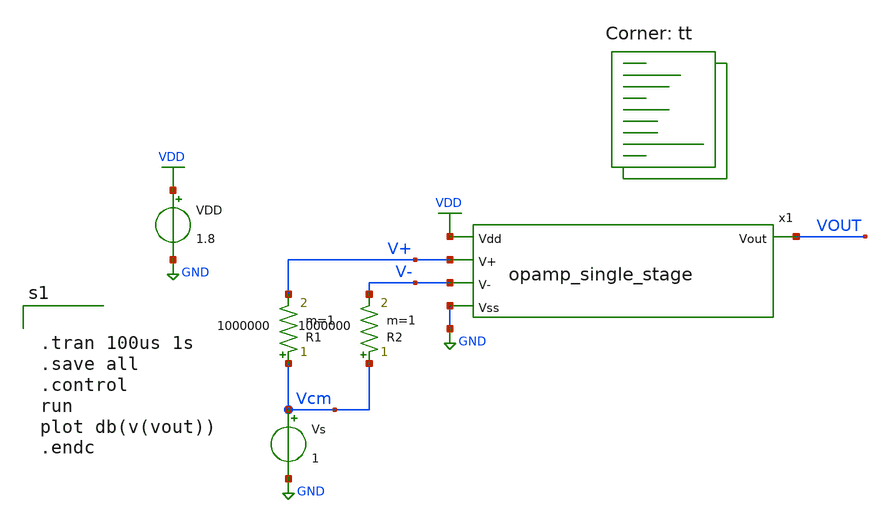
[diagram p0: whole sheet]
** sch_path: analog/schematics/tb_cmrr.sch
**.subckt tb_cmrr
VDD VDD GND 1.8
Vs Vcm GND 1
R1 Vcm V+ 1000000 m=1
R2 Vcm V- 1000000 m=1
x1 VDD VOUT V+ V- GND opamp_single_stage
**** begin user architecture code


.tran 100us 1s
.save all
.control
run
plot db(v(vout))
.endc


.lib $::SKYWATER_MODELS/sky130.lib.spice tt
**** end user architecture code
**.ends

* expanding   symbol:  opamp_single_stage.sym # of pins=5
** sym_path: analog/schematics/opamp_single_stage.sym
** sch_path: analog/schematics/opamp_single_stage.sch
.subckt opamp_single_stage Vdd Vout V+ V- Vss
*.opin Vout
*.ipin Vdd
*.ipin Vss
*.ipin V+
*.ipin V-
XM3 net1 V+ net2 Vss sky130_fd_pr__nfet_01v8 L=0.25 W=1 nf=1 ad='int((nf+1)/2) * W/nf * 0.29' as='int((nf+2)/2) * W/nf * 0.29'
+ pd='2*int((nf+1)/2) * (W/nf + 0.29)' ps='2*int((nf+2)/2) * (W/nf + 0.29)' nrd='0.29 / W' nrs='0.29 / W'
+ sa=0 sb=0 sd=0 mult=1 m=1
XM4 Vout V- net2 Vss sky130_fd_pr__nfet_01v8 L=0.25 W=1 nf=1 ad='int((nf+1)/2) * W/nf * 0.29' as='int((nf+2)/2) * W/nf * 0.29'
+ pd='2*int((nf+1)/2) * (W/nf + 0.29)' ps='2*int((nf+2)/2) * (W/nf + 0.29)' nrd='0.29 / W' nrs='0.29 / W'
+ sa=0 sb=0 sd=0 mult=1 m=1
XM5 net2 net3 Vss Vss sky130_fd_pr__nfet_01v8 L=0.25 W=1 nf=1 ad='int((nf+1)/2) * W/nf * 0.29' as='int((nf+2)/2) * W/nf * 0.29'
+ pd='2*int((nf+1)/2) * (W/nf + 0.29)' ps='2*int((nf+2)/2) * (W/nf + 0.29)' nrd='0.29 / W' nrs='0.29 / W'
+ sa=0 sb=0 sd=0 mult=1 m=1
XM1 net1 net1 Vdd Vdd sky130_fd_pr__pfet_01v8 L=0.25 W=1 nf=1 ad='int((nf+1)/2) * W/nf * 0.29' as='int((nf+2)/2) * W/nf * 0.29'
+ pd='2*int((nf+1)/2) * (W/nf + 0.29)' ps='2*int((nf+2)/2) * (W/nf + 0.29)' nrd='0.29 / W' nrs='0.29 / W'
+ sa=0 sb=0 sd=0 mult=1 m=1
XM2 Vout net1 Vdd Vdd sky130_fd_pr__pfet_01v8 L=0.25 W=1 nf=1 ad='int((nf+1)/2) * W/nf * 0.29' as='int((nf+2)/2) * W/nf * 0.29'
+ pd='2*int((nf+1)/2) * (W/nf + 0.29)' ps='2*int((nf+2)/2) * (W/nf + 0.29)' nrd='0.29 / W' nrs='0.29 / W'
+ sa=0 sb=0 sd=0 mult=1 m=1
XM6 net3 net3 Vss Vss sky130_fd_pr__nfet_01v8 L=0.25 W=1 nf=1 ad='int((nf+1)/2) * W/nf * 0.29' as='int((nf+2)/2) * W/nf * 0.29'
+ pd='2*int((nf+1)/2) * (W/nf + 0.29)' ps='2*int((nf+2)/2) * (W/nf + 0.29)' nrd='0.29 / W' nrs='0.29 / W'
+ sa=0 sb=0 sd=0 mult=1 m=1
XR1 net3 Vdd net4 sky130_fd_pr__res_high_po W=2.5 L=0.1 mult=1 m=1
.ends

.GLOBAL GND
.GLOBAL VDD
.end
